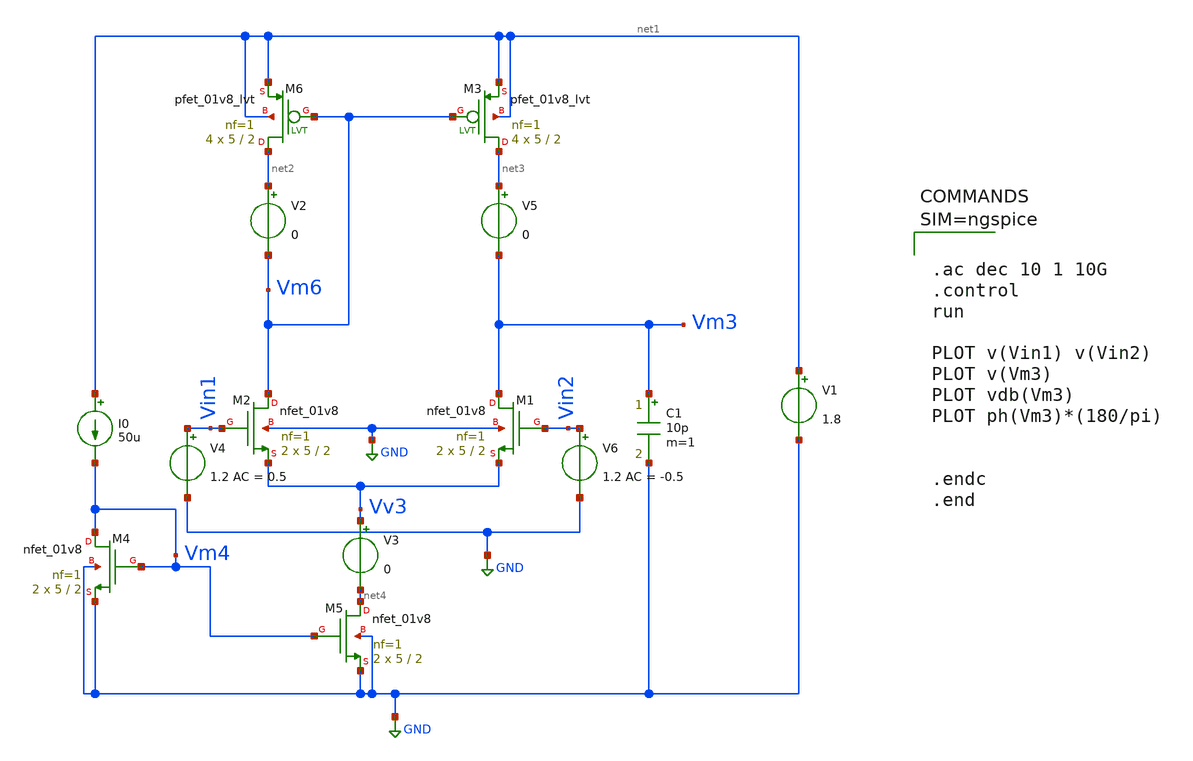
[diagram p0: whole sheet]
** sch_path: sch/Diff_Amplifier.sch
**.subckt Diff_Amplifier
XM2 Vm6 Vin1 Vv3 GND sky130_fd_pr__nfet_01v8 L=2 W=5 nf=1 ad='int((1 + 1)/2) * 5 / 1 * 0.29' as='int((1 + 2)/2) * 5 / 1 * 0.29'
+ pd='2*int((1 + 1)/2) * (5 / 1 + 0.29)' ps='2*int((1 + 2)/2) * (5 / 1 + 0.29)' nrd='0.29 / 5 ' nrs='0.29 / 5 '
+ sa=0 sb=0 sd=0 mult=2 m=2
XM1 Vm3 Vin2 Vv3 GND sky130_fd_pr__nfet_01v8 L=2 W=5 nf=1 ad='int((1 + 1)/2) * 5 / 1 * 0.29' as='int((1 + 2)/2) * 5 / 1 * 0.29'
+ pd='2*int((1 + 1)/2) * (5 / 1 + 0.29)' ps='2*int((1 + 2)/2) * (5 / 1 + 0.29)' nrd='0.29 / 5 ' nrs='0.29 / 5 '
+ sa=0 sb=0 sd=0 mult=2 m=2
XM6 net2 Vm6 net1 net1 sky130_fd_pr__pfet_01v8_lvt L=2 W=5 nf=1 ad='int((1 + 1)/2) * 5 / 1 * 0.29' as='int((1 + 2)/2) * 5 / 1 * 0.29'
+ pd='2*int((1 + 1)/2) * (5 / 1 + 0.29)' ps='2*int((1 + 2)/2) * (5 / 1 + 0.29)' nrd='0.29 / 5 ' nrs='0.29 / 5 '
+ sa=0 sb=0 sd=0 mult=4 m=4
XM3 net3 Vm6 net1 net1 sky130_fd_pr__pfet_01v8_lvt L=2 W=5 nf=1 ad='int((1 + 1)/2) * 5 / 1 * 0.29' as='int((1 + 2)/2) * 5 / 1 * 0.29'
+ pd='2*int((1 + 1)/2) * (5 / 1 + 0.29)' ps='2*int((1 + 2)/2) * (5 / 1 + 0.29)' nrd='0.29 / 5 ' nrs='0.29 / 5 '
+ sa=0 sb=0 sd=0 mult=4 m=4
XM4 Vm4 Vm4 GND GND sky130_fd_pr__nfet_01v8 L=2 W=5 nf=1 ad='int((1 + 1)/2) * 5 / 1 * 0.29' as='int((1 + 2)/2) * 5 / 1 * 0.29'
+ pd='2*int((1 + 1)/2) * (5 / 1 + 0.29)' ps='2*int((1 + 2)/2) * (5 / 1 + 0.29)' nrd='0.29 / 5 ' nrs='0.29 / 5 '
+ sa=0 sb=0 sd=0 mult=2 m=2
XM5 net4 Vm4 GND GND sky130_fd_pr__nfet_01v8 L=2 W=5 nf=1 ad='int((1 + 1)/2) * 5 / 1 * 0.29' as='int((1 + 2)/2) * 5 / 1 * 0.29'
+ pd='2*int((1 + 1)/2) * (5 / 1 + 0.29)' ps='2*int((1 + 2)/2) * (5 / 1 + 0.29)' nrd='0.29 / 5 ' nrs='0.29 / 5 '
+ sa=0 sb=0 sd=0 mult=2 m=2
I0 net1 Vm4 50u
C1 Vm3 GND 10p m=1
V1 net1 GND 1.8
V2 net2 Vm6 0
V3 Vv3 net4 0
V5 net3 Vm3 0
V4 Vin1 GND 1.2 AC = 0.5
V6 Vin2 GND 1.2 AC = -0.5
**** begin user architecture code

** opencircuitdesign pdks install
.lib $::SKYWATER_MODELS/sky130.lib.spice tt




.ac dec 10 1 10G
.control
run

PLOT v(Vin1) v(Vin2)
PLOT v(Vm3)
PLOT vdb(Vm3)
PLOT ph(Vm3)*(180/pi)


.endc
.end



**** end user architecture code
**.ends
.GLOBAL GND
.end
